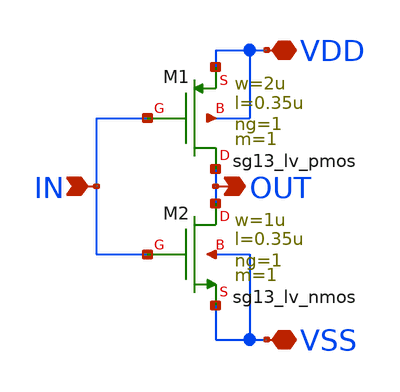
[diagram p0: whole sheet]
** sch_path: macros/heichips26_chronosense/schematic/xschem/inv.sch
* Copyright 2023 IHP PDK Authors
* Licensed under the Apache License, Version 2.0 (the "License");
* you may not use this file except in compliance with the License.
* You may obtain a copy of the License at
* https://www.apache.org/licenses/LICENSE-2.0
* Unless required by applicable law or agreed to in writing, software
* distributed under the License is distributed on an "AS IS" BASIS,
* WITHOUT WARRANTIES OR CONDITIONS OF ANY KIND, either express or implied.
* See the License for the specific language governing permissions and
* limitations under the License.
**.subckt inv IN OUT VDD VSS
*.ipin IN
*.opin OUT
*.iopin VDD
*.iopin VSS
XM1 OUT IN VDD VDD sg13_lv_pmos w=2u l=0.35u ng=1 m=1 mm_ok=1
XM2 OUT IN VSS VSS sg13_lv_nmos w=1u l=0.35u ng=1 m=1 mm_ok=1
**.ends
.end
